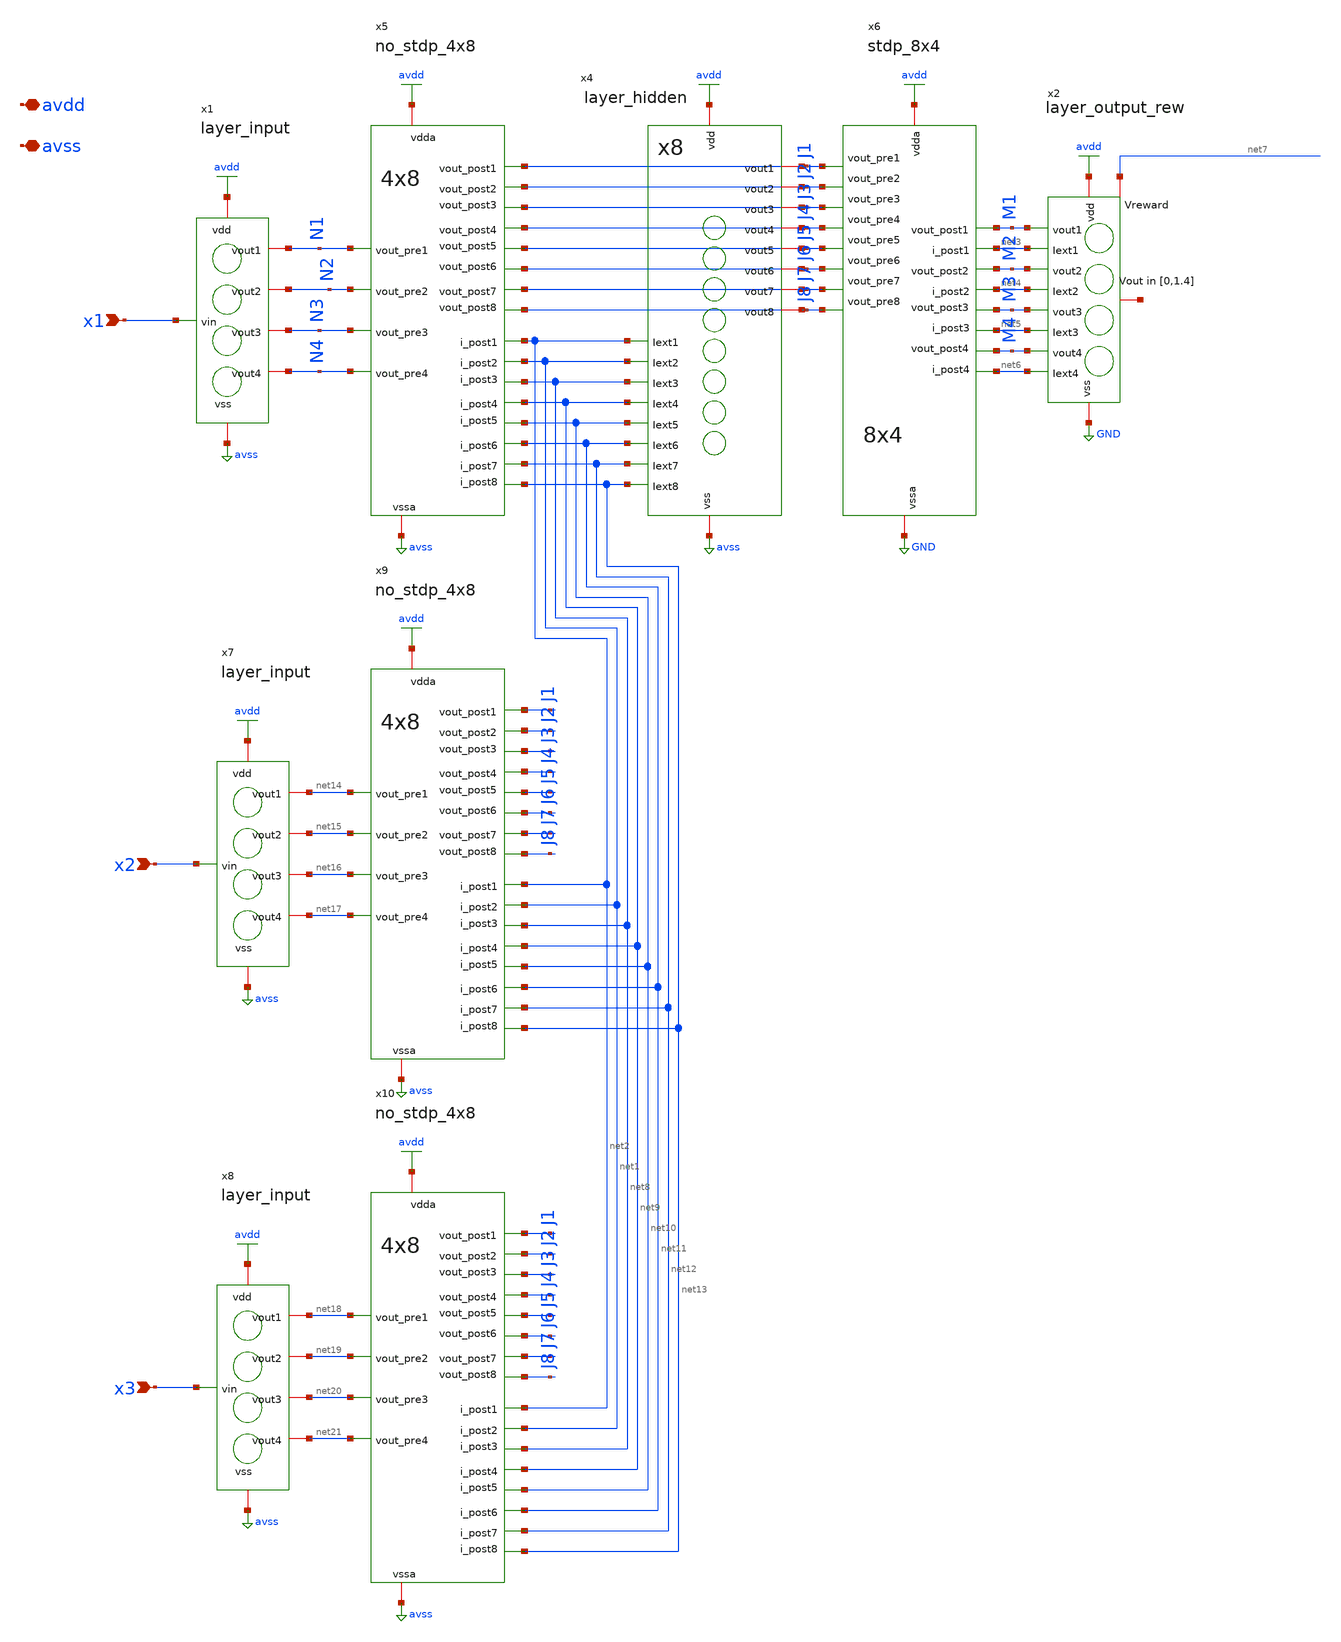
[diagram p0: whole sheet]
** sch_path: untitled.sch
**.subckt untitled x1 x3 x2 avdd avss
*.ipin x1
*.ipin x3
*.ipin x2
*.iopin avdd
*.iopin avss
x1 avdd avss x1 N1 N2 N3 N4 layer_input
x4 avdd net2 avss net1 net8 J1 J2 net9 J3 net10 J4 net11 J5 net12 J6 J7 net13 J8 layer_hidden
x5 avdd net2 net1 net8 avss J1 J2 net12 net13 net10 J3 net9 net11 J8 J7 J6 J5 J4 N1 N2 N3 N4
+ no_stdp_4x8
x6 net4 net3 M2 net5 GND M1 M3 net6 M4 J1 J2 J3 J4 J5 J6 J7 J8 avdd stdp_8x4
x2 avdd net3 GND net4 net5 net22 net6 M1 M2 M3 M4 net7 layer_output_rew
x7 avdd avss x2 net14 net15 net16 net17 layer_input
x8 avdd avss x3 net18 net19 net20 net21 layer_input
x9 avdd net2 net1 net8 avss J1 J2 net12 net13 net10 J3 net9 net11 J8 J7 J6 J5 J4 net14 net15 net16
+ net17 no_stdp_4x8
x10 avdd net2 net1 net8 avss J1 J2 net12 net13 net10 J3 net9 net11 J8 J7 J6 J5 J4 net18 net19 net20
+ net21 no_stdp_4x8
**.ends
.GLOBAL avss
.GLOBAL avdd
.GLOBAL GND
.end
